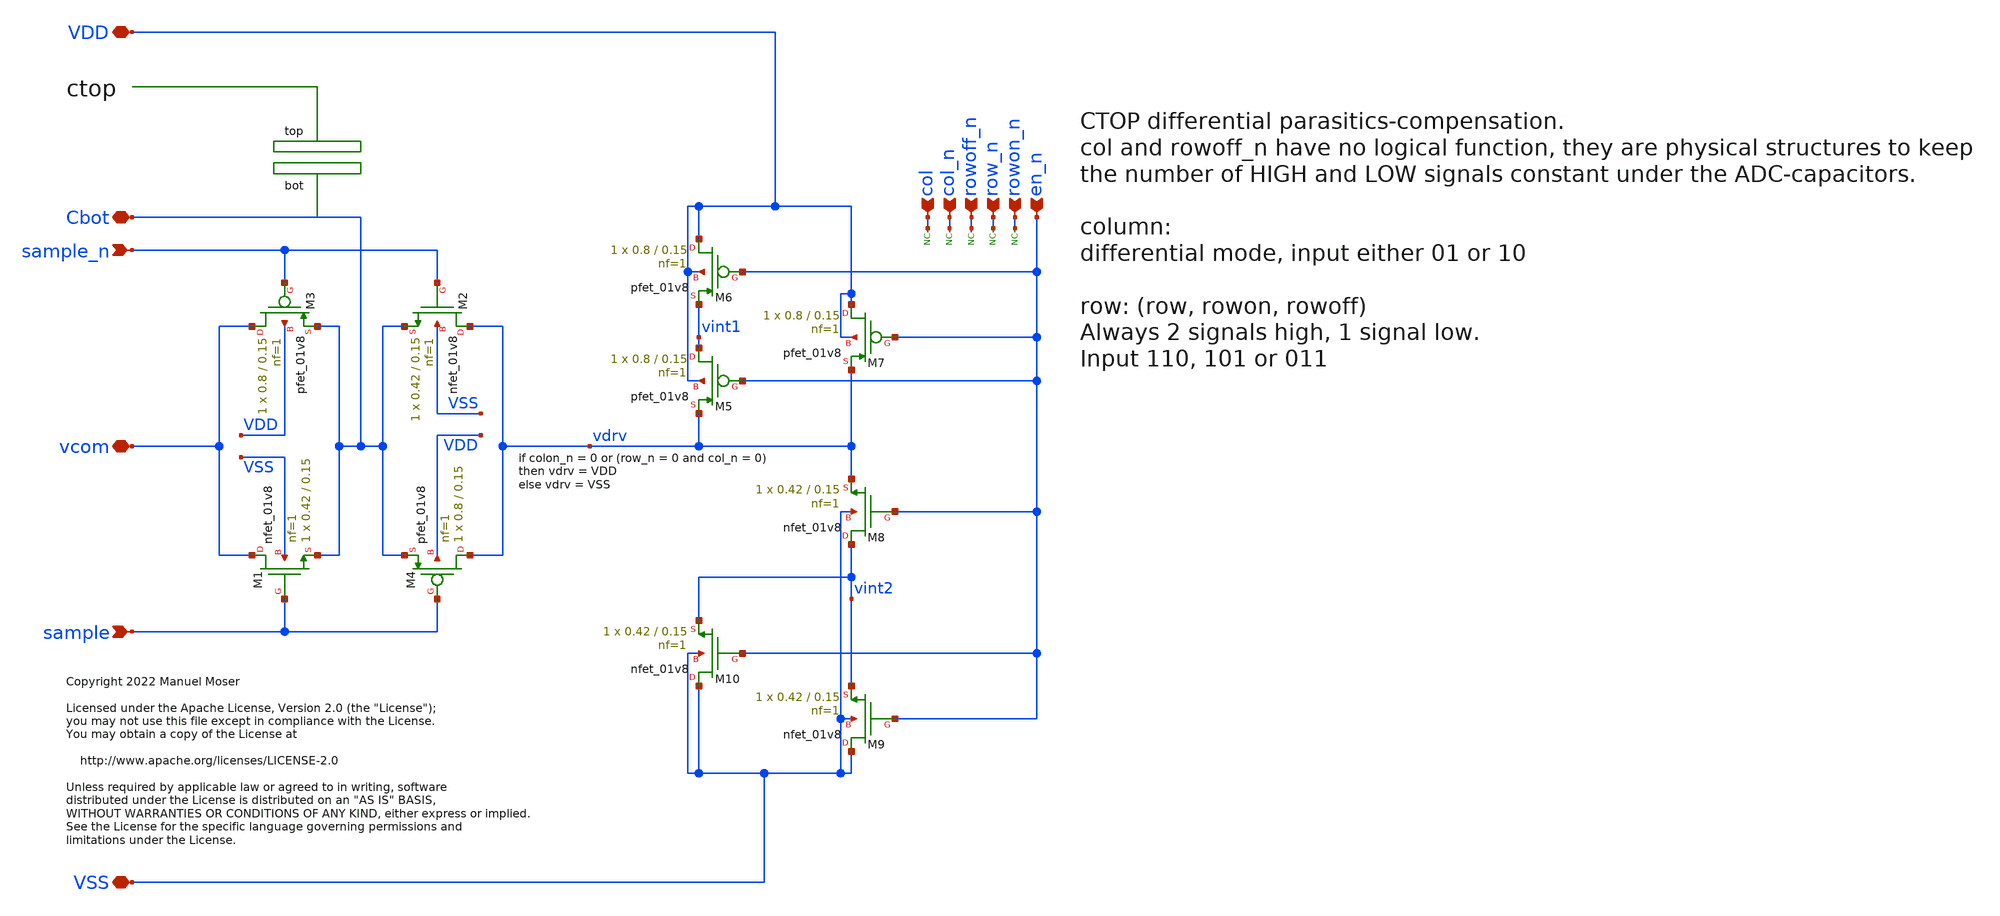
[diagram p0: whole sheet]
** sch_path: xschem/adc_array_circuit_4.sch
* Copyright 2022 Manuel Moser
* Licensed under the Apache License, Version 2.0 (the "License");
**.subckt adc_array_circuit_4 sample_n sample vcom rowoff_n row_n rowon_n VDD VSS Cbot en_n col_n
*+ col
*.ipin sample_n
*.ipin sample
*.iopin vcom
*.ipin rowoff_n
*.ipin row_n
*.ipin rowon_n
*.iopin VDD
*.iopin VSS
*.iopin Cbot
*.ipin en_n
*.ipin col_n
*.ipin col
XM1 vcom sample Cbot VSS sky130_fd_pr__nfet_01v8 L=0.15 W=0.42 nf=1 ad='int((nf+1)/2) * W/nf * 0.29'
+ as='int((nf+2)/2) * W/nf * 0.29' pd='2*int((nf+1)/2) * (W/nf + 0.29)' ps='2*int((nf+2)/2) * (W/nf + 0.29)'
+ nrd='0.29 / W' nrs='0.29 / W' sa=0 sb=0 sd=0 mult=1 m=1
XM3 vcom sample_n Cbot VDD sky130_fd_pr__pfet_01v8 L=0.15 W=0.8 nf=1 ad='int((nf+1)/2) * W/nf * 0.29'
+ as='int((nf+2)/2) * W/nf * 0.29' pd='2*int((nf+1)/2) * (W/nf + 0.29)' ps='2*int((nf+2)/2) * (W/nf + 0.29)'
+ nrd='0.29 / W' nrs='0.29 / W' sa=0 sb=0 sd=0 mult=1 m=1
XM2 vdrv sample_n Cbot VSS sky130_fd_pr__nfet_01v8 L=0.15 W=0.42 nf=1 ad='int((nf+1)/2) * W/nf * 0.29'
+ as='int((nf+2)/2) * W/nf * 0.29' pd='2*int((nf+1)/2) * (W/nf + 0.29)' ps='2*int((nf+2)/2) * (W/nf + 0.29)'
+ nrd='0.29 / W' nrs='0.29 / W' sa=0 sb=0 sd=0 mult=1 m=1
XM4 vdrv sample Cbot VDD sky130_fd_pr__pfet_01v8 L=0.15 W=0.8 nf=1 ad='int((nf+1)/2) * W/nf * 0.29' as='int((nf+2)/2) * W/nf * 0.29'
+ pd='2*int((nf+1)/2) * (W/nf + 0.29)' ps='2*int((nf+2)/2) * (W/nf + 0.29)' nrd='0.29 / W' nrs='0.29 / W'
+ sa=0 sb=0 sd=0 mult=1 m=1
XM5 vint1 en_n vdrv VDD sky130_fd_pr__pfet_01v8 L=0.15 W=0.8 nf=1 ad='int((nf+1)/2) * W/nf * 0.29' as='int((nf+2)/2) * W/nf * 0.29'
+ pd='2*int((nf+1)/2) * (W/nf + 0.29)' ps='2*int((nf+2)/2) * (W/nf + 0.29)' nrd='0.29 / W' nrs='0.29 / W'
+ sa=0 sb=0 sd=0 mult=1 m=1
XM6 VDD en_n vint1 VDD sky130_fd_pr__pfet_01v8 L=0.15 W=0.8 nf=1 ad='int((nf+1)/2) * W/nf * 0.29' as='int((nf+2)/2) * W/nf * 0.29'
+ pd='2*int((nf+1)/2) * (W/nf + 0.29)' ps='2*int((nf+2)/2) * (W/nf + 0.29)' nrd='0.29 / W' nrs='0.29 / W'
+ sa=0 sb=0 sd=0 mult=1 m=1
XM7 VDD en_n vdrv VDD sky130_fd_pr__pfet_01v8 L=0.15 W=0.8 nf=1 ad='int((nf+1)/2) * W/nf * 0.29' as='int((nf+2)/2) * W/nf * 0.29'
+ pd='2*int((nf+1)/2) * (W/nf + 0.29)' ps='2*int((nf+2)/2) * (W/nf + 0.29)' nrd='0.29 / W' nrs='0.29 / W'
+ sa=0 sb=0 sd=0 mult=1 m=1
XM8 vint2 en_n vdrv VSS sky130_fd_pr__nfet_01v8 L=0.15 W=0.42 nf=1 ad='int((nf+1)/2) * W/nf * 0.29' as='int((nf+2)/2) * W/nf * 0.29'
+ pd='2*int((nf+1)/2) * (W/nf + 0.29)' ps='2*int((nf+2)/2) * (W/nf + 0.29)' nrd='0.29 / W' nrs='0.29 / W'
+ sa=0 sb=0 sd=0 mult=1 m=1
XM9 VSS en_n vint2 VSS sky130_fd_pr__nfet_01v8 L=0.15 W=0.42 nf=1 ad='int((nf+1)/2) * W/nf * 0.29' as='int((nf+2)/2) * W/nf * 0.29'
+ pd='2*int((nf+1)/2) * (W/nf + 0.29)' ps='2*int((nf+2)/2) * (W/nf + 0.29)' nrd='0.29 / W' nrs='0.29 / W'
+ sa=0 sb=0 sd=0 mult=1 m=1
XM10 VSS en_n vint2 VSS sky130_fd_pr__nfet_01v8 L=0.15 W=0.42 nf=1 ad='int((nf+1)/2) * W/nf * 0.29' as='int((nf+2)/2) * W/nf * 0.29'
+ pd='2*int((nf+1)/2) * (W/nf + 0.29)' ps='2*int((nf+2)/2) * (W/nf + 0.29)' nrd='0.29 / W' nrs='0.29 / W'
+ sa=0 sb=0 sd=0 mult=1 m=1
* noconn rowoff_n
* noconn row_n
* noconn rowon_n
* noconn col_n
* noconn col
**.ends
.end
